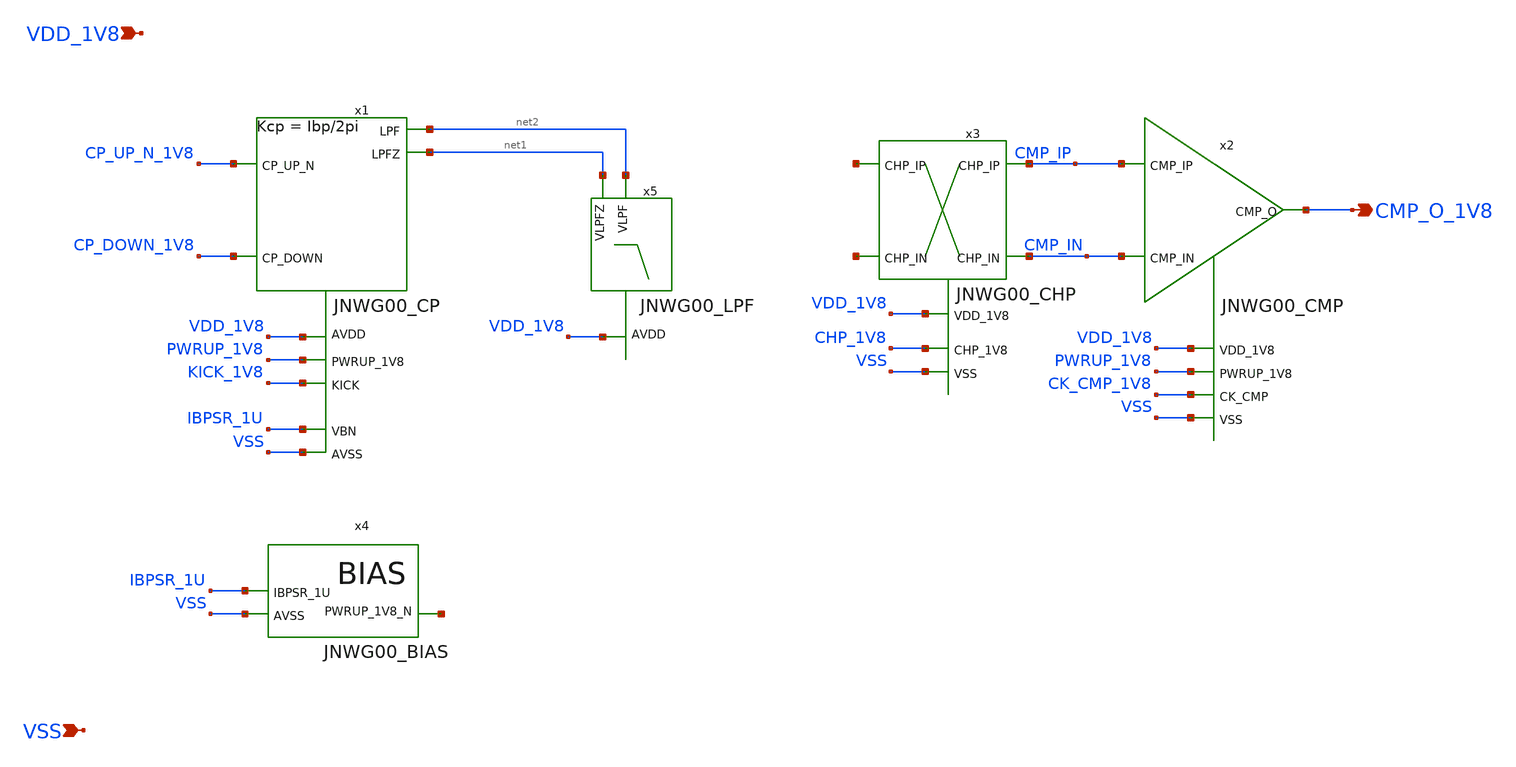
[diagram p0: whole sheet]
** sch_path: design/JNW_GR00_SKY130NM/JNWG00_ANA.sch
**.subckt JNWG00_ANA VDD_1V8 VSS CMP_O_1V8
*.ipin VDD_1V8
*.ipin VSS
*.opin CMP_O_1V8
x1 VDD_1V8 CP_UP_N_1V8 net2 CP_DOWN_1V8 IBPSR_1U VSS net1 PWRUP_1V8 KICK_1V8 JNWG00_CP
x2 VDD_1V8 PWRUP_1V8 CMP_IP CMP_O_1V8 CMP_IN CK_CMP_1V8 VSS JNWG00_CMP
x3 VDD_1V8 CMP_IP CMP_IN CHP_1V8 VSS JNWG00_CHP
x4 IBPSR_1U net3 VSS JNWG00_BIAS
x5 net1 VDD_1V8 net2 JNWG00_LPF
**.ends
.end
